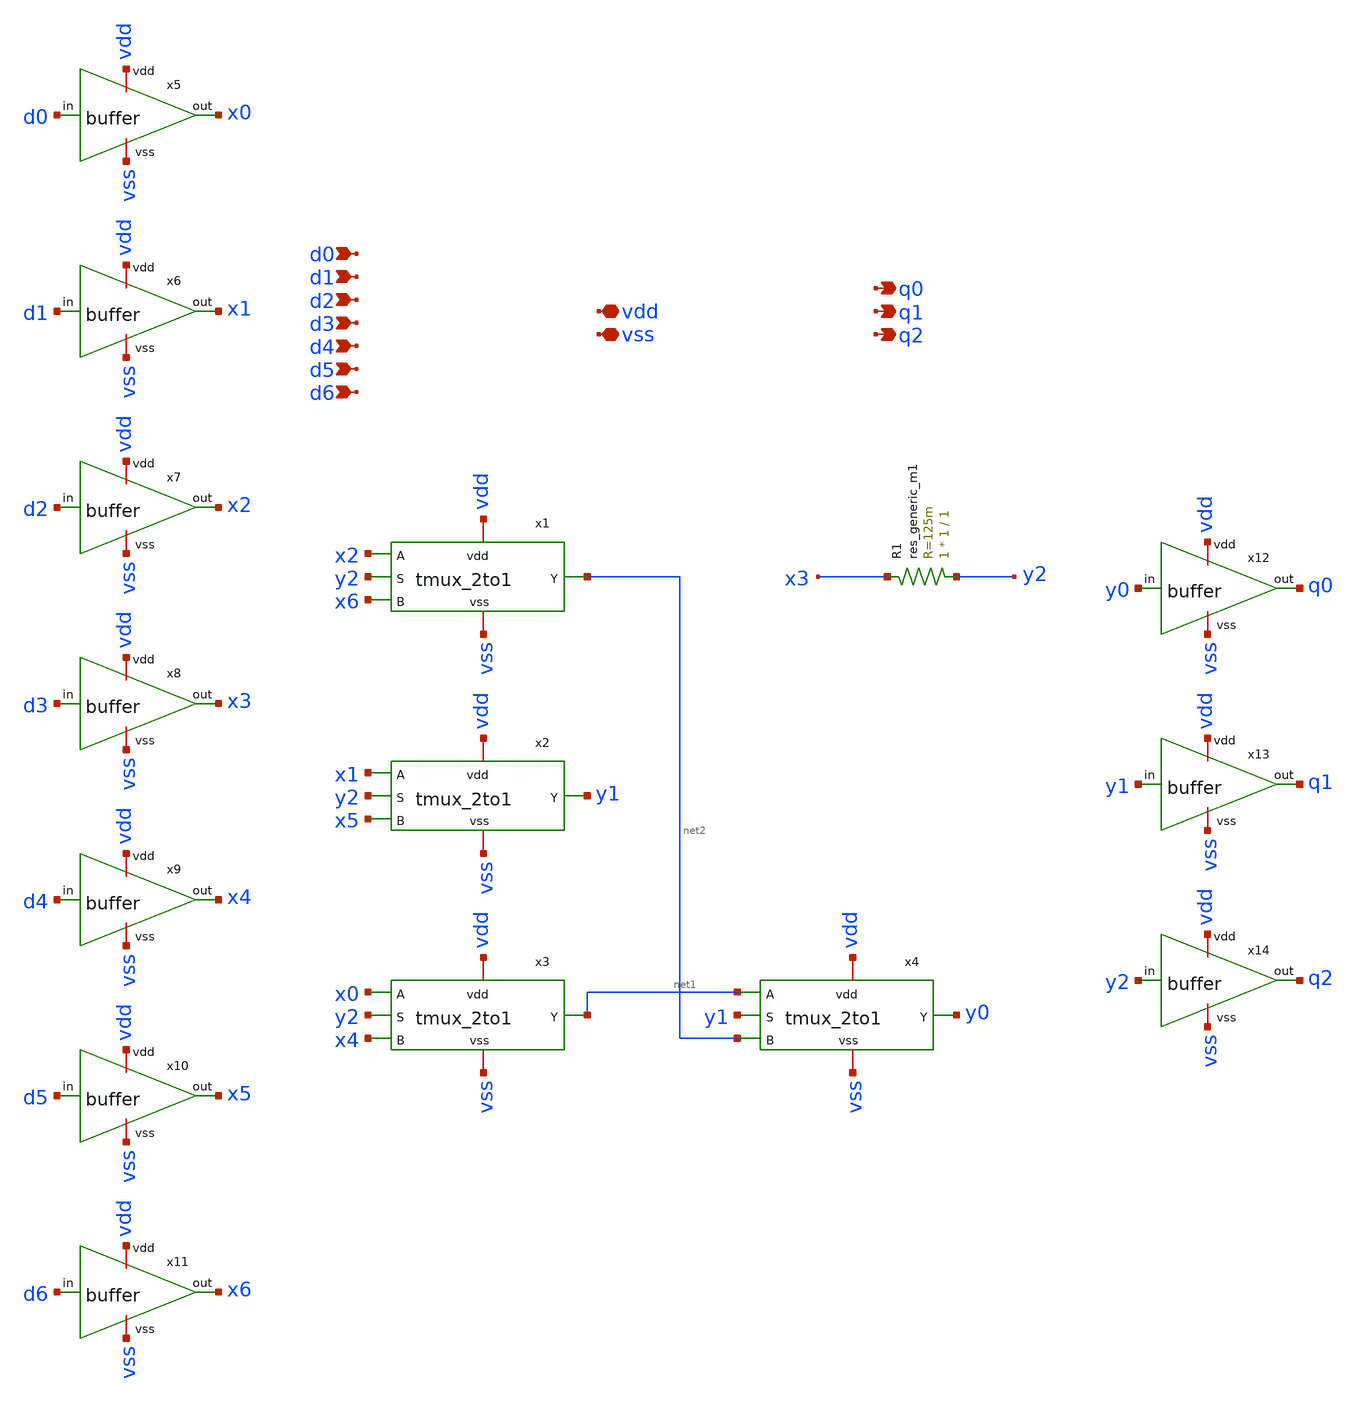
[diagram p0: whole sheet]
** sch_path: xsch/ip/tmux_encoder/tmux_7therm_to_3bin.sch
**.subckt tmux_7therm_to_3bin d0 vdd q0 d1 d2 d3 d4 d5 d6 q1 q2 vss
*.ipin d0
*.iopin vdd
*.opin q0
*.ipin d1
*.ipin d2
*.ipin d3
*.ipin d4
*.ipin d5
*.ipin d6
*.opin q1
*.opin q2
*.iopin vss
R1 y2 x3 sky130_fd_pr__res_generic_m1 W=1 L=1 m=1
x1 x2 x6 y2 net2 vdd vss tmux_2to1
x2 x1 x5 y2 y1 vdd vss tmux_2to1
x3 x0 x4 y2 net1 vdd vss tmux_2to1
x4 net1 net2 y1 y0 vdd vss tmux_2to1
x5 d0 x0 vdd vss buffer
x6 d1 x1 vdd vss buffer
x7 d2 x2 vdd vss buffer
x8 d3 x3 vdd vss buffer
x9 d4 x4 vdd vss buffer
x10 d5 x5 vdd vss buffer
x11 d6 x6 vdd vss buffer
x12 y0 q0 vdd vss buffer
x13 y1 q1 vdd vss buffer
x14 y2 q2 vdd vss buffer
**.ends

* expanding   symbol:  /home/bmott/ttsky25b_tiny_chaos/xsch/ip/tmux/tmux_2to1.sym # of pins=6
** sym_path: xsch/ip/tmux/tmux_2to1.sym
** sch_path: xsch/ip/tmux/tmux_2to1.sch
.subckt tmux_2to1 A B S Y vdd vss
*.opin Y
*.ipin S
*.iopin vss
*.iopin vdd
*.ipin A
*.ipin B
XM1 net1 S vdd vdd sky130_fd_pr__pfet_01v8 L=0.15 W=2 nf=1 ad='int((1 + 1)/2) * 2 / 1 * 0.29' as='int((1 + 2)/2) * 2 / 1 * 0.29'
+ pd='2*int((1 + 1)/2) * (2 / 1 + 0.29)' ps='2*int((1 + 2)/2) * (2 / 1 + 0.29)' nrd='0.29 / 2 ' nrs='0.29 / 2 '
+ sa=0 sb=0 sd=0 mult=1 m=1
XM2 net1 S vss vss sky130_fd_pr__nfet_01v8 L=0.15 W=1 nf=1 ad='int((1 + 1)/2) * 1 / 1 * 0.29' as='int((1 + 2)/2) * 1 / 1 * 0.29'
+ pd='2*int((1 + 1)/2) * (1 / 1 + 0.29)' ps='2*int((1 + 2)/2) * (1 / 1 + 0.29)' nrd='0.29 / 1 ' nrs='0.29 / 1 '
+ sa=0 sb=0 sd=0 mult=1 m=1
XM3 B net1 Y vdd sky130_fd_pr__pfet_01v8 L=0.15 W=2 nf=1 ad='int((1 + 1)/2) * 2 / 1 * 0.29' as='int((1 + 2)/2) * 2 / 1 * 0.29'
+ pd='2*int((1 + 1)/2) * (2 / 1 + 0.29)' ps='2*int((1 + 2)/2) * (2 / 1 + 0.29)' nrd='0.29 / 2 ' nrs='0.29 / 2 '
+ sa=0 sb=0 sd=0 mult=1 m=1
XM4 B S Y vss sky130_fd_pr__nfet_01v8 L=0.15 W=1 nf=1 ad='int((1 + 1)/2) * 1 / 1 * 0.29' as='int((1 + 2)/2) * 1 / 1 * 0.29'
+ pd='2*int((1 + 1)/2) * (1 / 1 + 0.29)' ps='2*int((1 + 2)/2) * (1 / 1 + 0.29)' nrd='0.29 / 1 ' nrs='0.29 / 1 '
+ sa=0 sb=0 sd=0 mult=1 m=1
XM5 A S Y vdd sky130_fd_pr__pfet_01v8 L=0.15 W=2 nf=1 ad='int((1 + 1)/2) * 2 / 1 * 0.29' as='int((1 + 2)/2) * 2 / 1 * 0.29'
+ pd='2*int((1 + 1)/2) * (2 / 1 + 0.29)' ps='2*int((1 + 2)/2) * (2 / 1 + 0.29)' nrd='0.29 / 2 ' nrs='0.29 / 2 '
+ sa=0 sb=0 sd=0 mult=1 m=1
XM6 A net1 Y vss sky130_fd_pr__nfet_01v8 L=0.15 W=1 nf=1 ad='int((1 + 1)/2) * 1 / 1 * 0.29' as='int((1 + 2)/2) * 1 / 1 * 0.29'
+ pd='2*int((1 + 1)/2) * (1 / 1 + 0.29)' ps='2*int((1 + 2)/2) * (1 / 1 + 0.29)' nrd='0.29 / 1 ' nrs='0.29 / 1 '
+ sa=0 sb=0 sd=0 mult=1 m=1
.ends


* expanding   symbol:  /home/bmott/ttsky25b_tiny_chaos/xsch/ip/logic/buffer/buffer.sym # of pins=4
** sym_path: xsch/ip/logic/buffer/buffer.sym
** sch_path: xsch/ip/logic/buffer/buffer.sch
.subckt buffer in out vdd vss
*.ipin in
*.opin out
*.iopin vdd
*.iopin vss
X1 in net1 vdd vss inv
X2 net1 out vdd vss inv
.ends


* expanding   symbol:  /home/bmott/ttsky25b_tiny_chaos/xsch/ip/logic/inv/inv.sym # of pins=4
** sym_path: xsch/ip/logic/inv/inv.sym
** sch_path: xsch/ip/logic/inv/inv.sch
.subckt inv vin vout vdd vss
*.ipin vin
*.opin vout
*.ipin vdd
*.ipin vss
XMn vout vin vss vss sky130_fd_pr__nfet_01v8 L=0.15 W=1 nf=1 ad='int((1 + 1)/2) * 1 / 1 * 0.29' as='int((1 + 2)/2) * 1 / 1 * 0.29'
+ pd='2*int((1 + 1)/2) * (1 / 1 + 0.29)' ps='2*int((1 + 2)/2) * (1 / 1 + 0.29)' nrd='0.29 / 1 ' nrs='0.29 / 1 '
+ sa=0 sb=0 sd=0 mult=1 m=1
XMp vout vin vdd vdd sky130_fd_pr__pfet_01v8 L=0.15 W=2 nf=1 ad='int((nf+1)/2) * W/nf * 0.29' as='int((nf+2)/2) * W/nf * 0.29'
+ pd='2*int((nf+1)/2) * (W/nf + 0.29)' ps='2*int((nf+2)/2) * (W/nf + 0.29)' nrd='0.29 / W' nrs='0.29 / W'
+ sa=0 sb=0 sd=0 mult=1 m=1
.ends

.end
